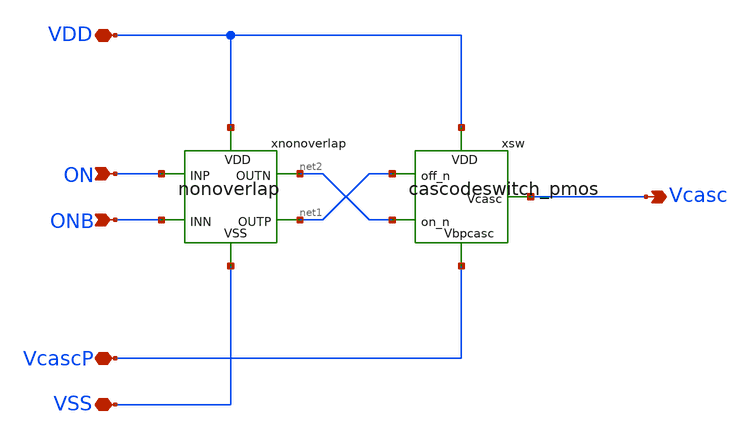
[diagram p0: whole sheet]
** sch_path: xschem/cascodedrive.sch
**.subckt cascodedrive VSS VDD VcascP ON ONB Vcasc
*.iopin VSS
*.iopin VDD
*.iopin VcascP
*.ipin ON
*.ipin ONB
*.opin Vcasc
xnonoverlap VDD VSS ON ONB net2 net1 nonoverlap
xsw VDD net1 Vcasc net2 VcascP cascodeswitch_pmos
**.ends

* expanding   symbol:  nonoverlap.sym # of pins=6
** sym_path: xschem/nonoverlap.sym
** sch_path: xschem/nonoverlap.sch
.subckt nonoverlap VDD VSS INP INN OUTN OUTP
*.iopin VSS
*.iopin VDD
*.ipin INP
*.ipin INN
*.opin OUTP
*.opin OUTN
XM1 OUTN INP VDD VDD sg13_lv_pmos w=0.3u l=0.13u ng=1 m=1 mm_ok=1
XM2 OUTP INN VDD VDD sg13_lv_pmos w=0.3u l=0.13u ng=1 m=1 mm_ok=1
XM3 OUTN OUTP VSS VSS sg13_lv_nmos w=0.15u l=0.52u ng=1 m=1 mm_ok=1
XM4 OUTP OUTN VSS VSS sg13_lv_nmos w=0.15u l=0.52u ng=1 m=1 mm_ok=1
.ends


* expanding   symbol:  cascodeswitch_pmos.sym # of pins=5
** sym_path: xschem/cascodeswitch_pmos.sym
** sch_path: xschem/cascodeswitch_pmos.sch
.subckt cascodeswitch_pmos VDD off_n Vcasc on_n Vbpcasc
*.ipin off_n
*.ipin Vbpcasc
*.opin Vcasc
*.ipin on_n
*.ipin VDD
XMpullup Vcasc off_n VDD VDD sg13_lv_pmos w=0.3u l=0.13u ng=1 m=1 mm_ok=1
XMbias Vbpcasc on_n Vcasc VDD sg13_lv_pmos w=0.3u l=0.13u ng=1 m=1 mm_ok=1
.ends

.end
